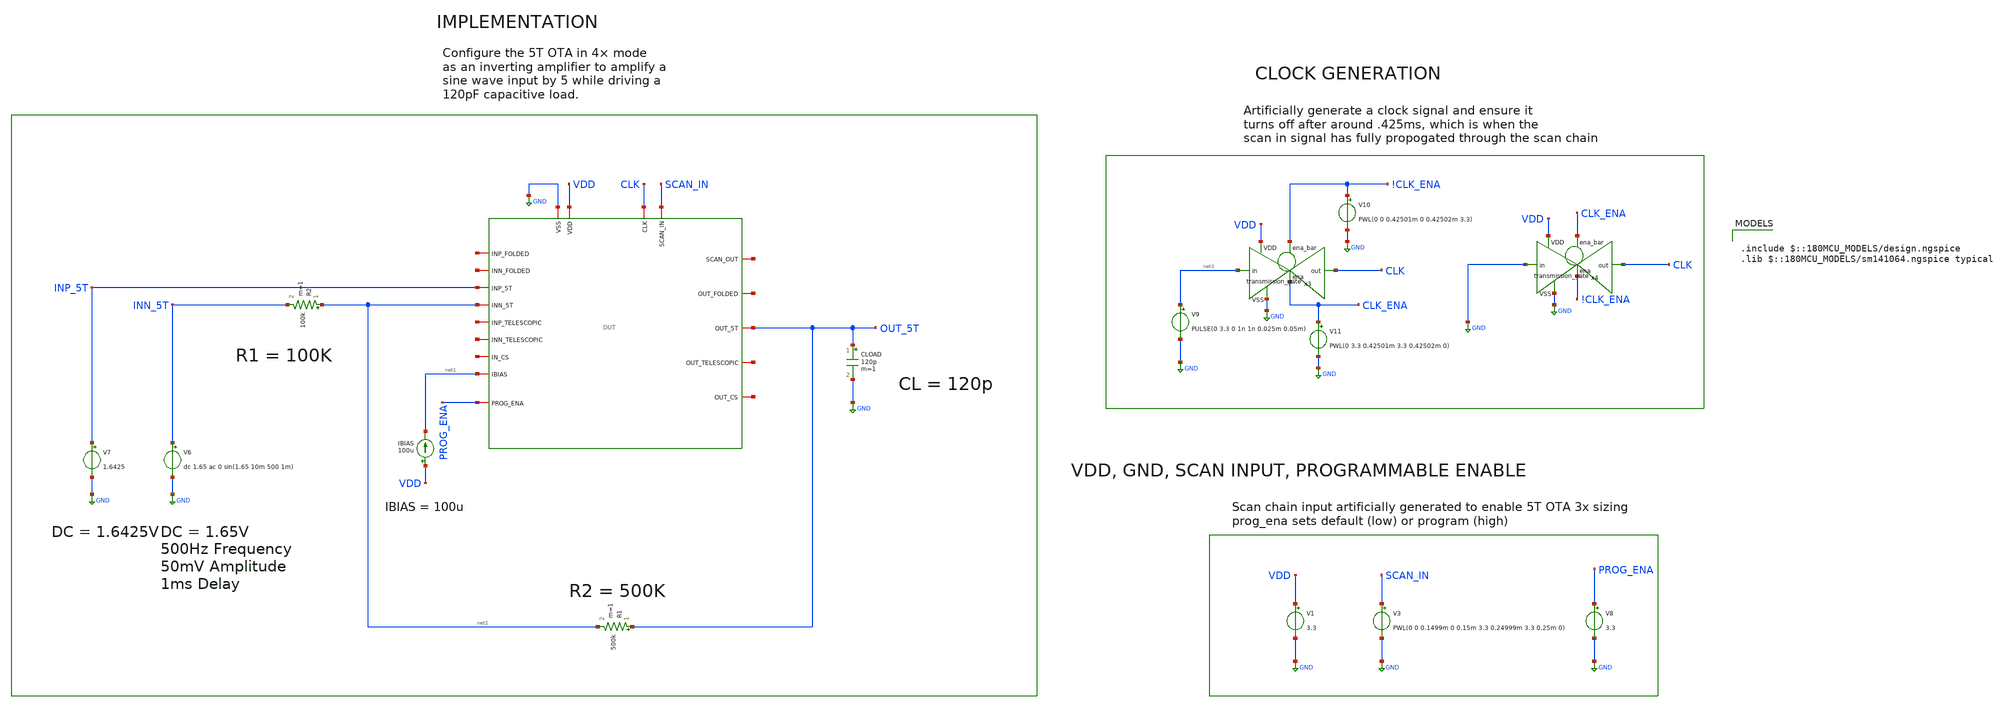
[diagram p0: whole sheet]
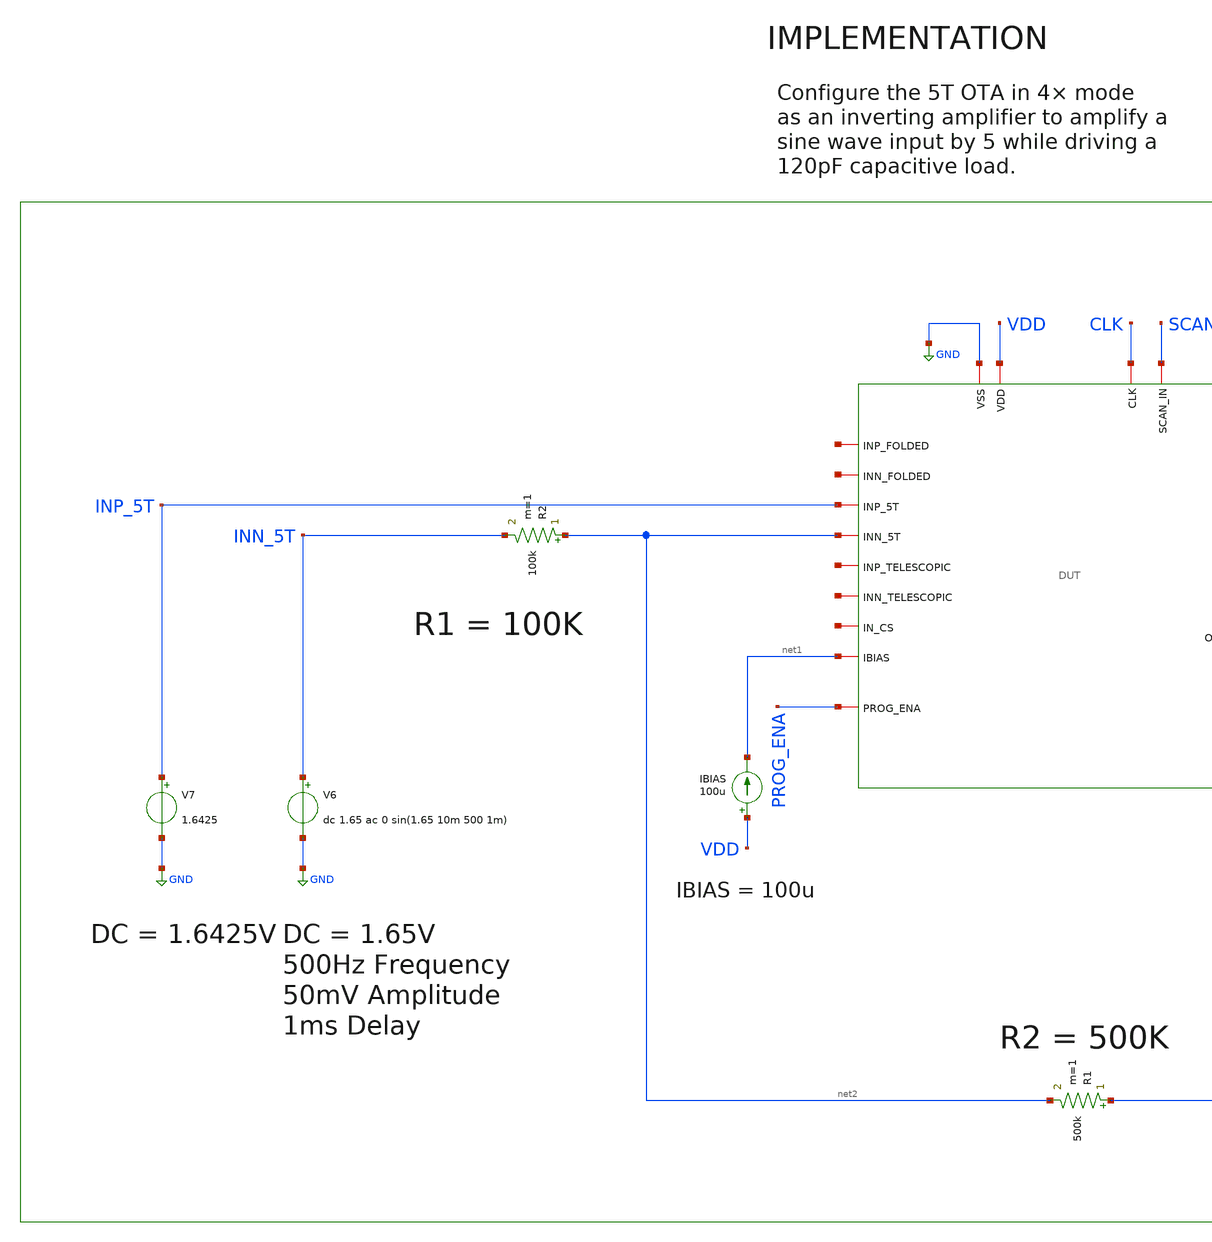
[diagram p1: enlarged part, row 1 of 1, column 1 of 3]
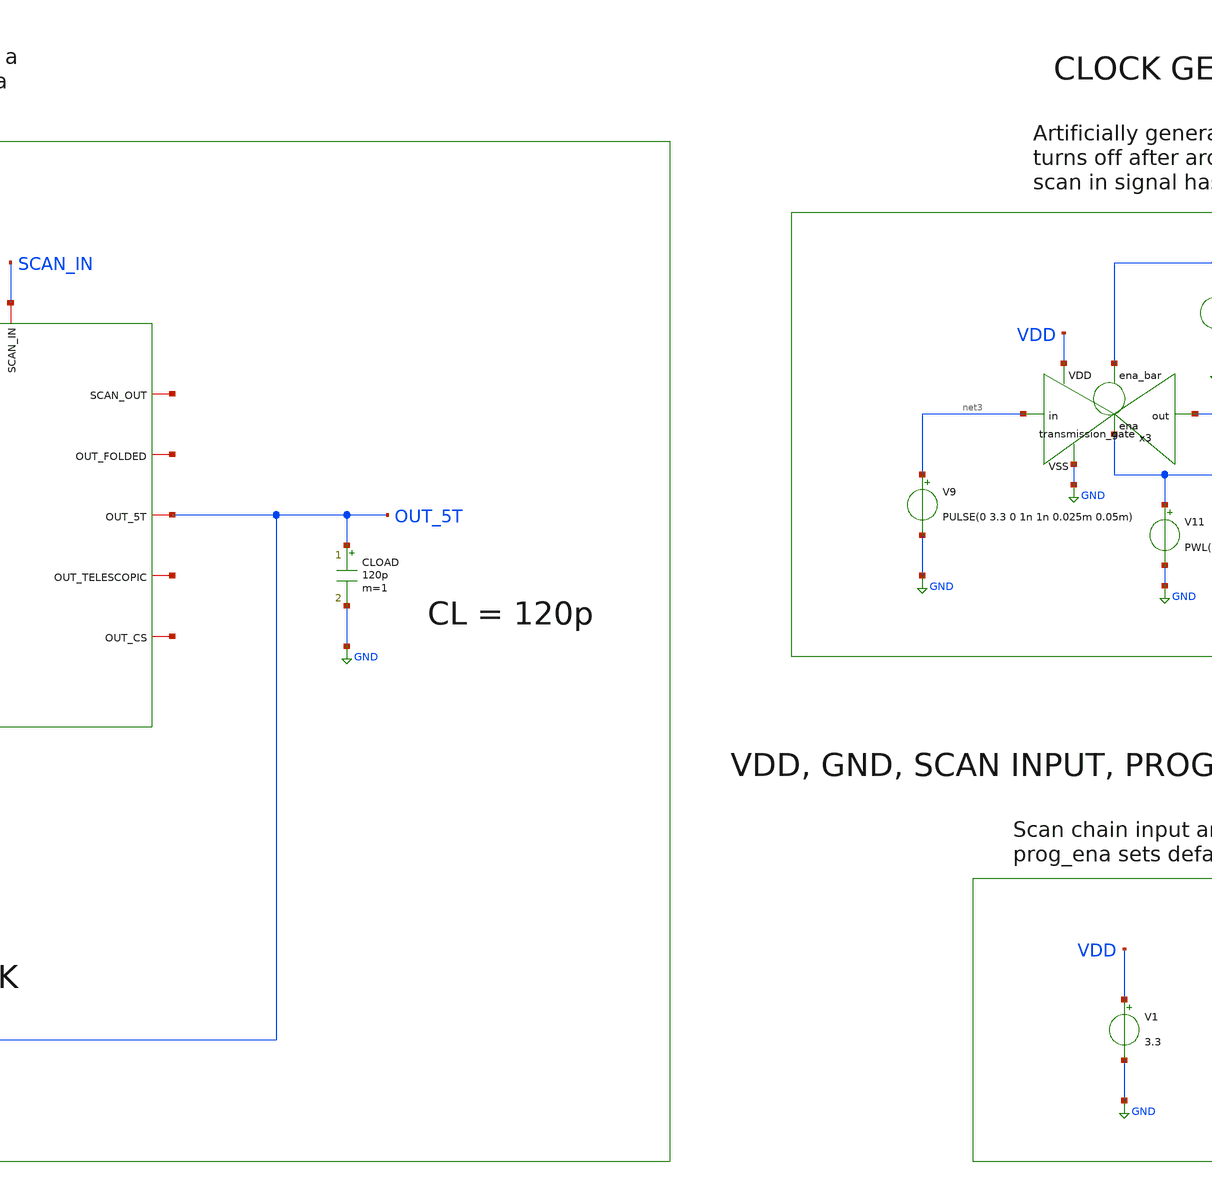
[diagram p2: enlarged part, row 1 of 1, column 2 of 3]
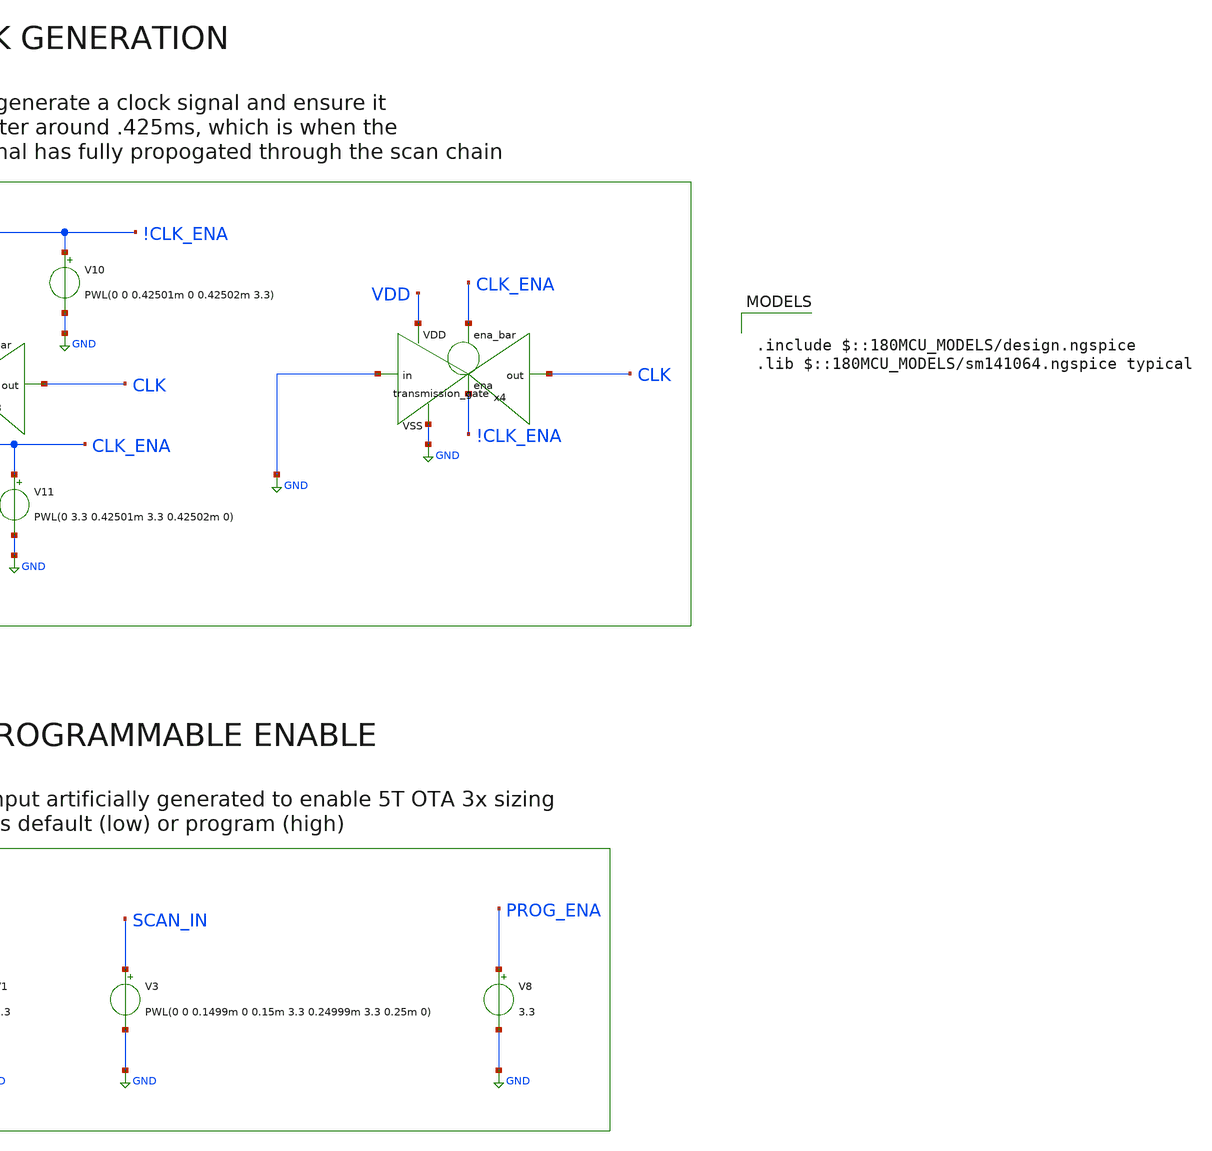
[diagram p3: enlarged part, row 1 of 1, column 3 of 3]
** sch_path: designs/libs/pex/5t/inverting_amplifier/4x.sch
**.subckt 4x
V3 SCAN_IN GND PWL(0 0 0.1499m 0 0.15m 3.3 0.24999m 3.3 0.25m 0)
V1 VDD GND 3.3
IBIAS VDD net1 100u
V7 INP_5T GND 1.6425
CLOAD OUT_5T GND 120p m=1
R2 net2 INN_5T 100k m=1
V6 INN_5T GND dc 1.65 ac 0 sin(1.65 10m 500 1m)
R1 OUT_5T net2 500k m=1
V8 PROG_ENA GND 3.3
V9 net3 GND PULSE(0 3.3 0 1n 1n 0.025m 0.05m)
x3 !CLK_ENA VDD CLK net3 GND CLK_ENA transmission_gate
V10 !CLK_ENA GND PWL(0 0 0.42501m 0 0.42502m 3.3)
V11 CLK_ENA GND PWL(0 3.3 0.42501m 3.3 0.42502m 0)
x4 CLK_ENA VDD CLK GND GND !CLK_ENA transmission_gate
x1 CLK net4 SCAN_IN GND VDD net5 net6 OUT_5T net1 net7 INP_5T net2 net8 net9 net10 net11 net12
+ PROG_ENA DUT
**** begin user architecture code

.include $::180MCU_MODELS/design.ngspice
.lib $::180MCU_MODELS/sm141064.ngspice typical



.include /foss/designs/libs/pex/DUT.spice
.control
tran 1u 5m

set color0 = white
set color1 = black

plot v(out_5T) v(inn_5T)

meas tran vout_pp pp v(out_5T) from=2m to=5m
meas tran vin_pp pp v(inn_5T) from=2m to=5m
let gain = vout_pp / vin_pp
print gain

meas tran vout_dc avg v(out_5T) from=2m to=5m
meas tran vin_dc avg v(inn_5T) from=2m to=5m
let dc_offset = vout_dc - vin_dc
let input_offset = dc_offset / 6
print vout_dc vin_dc dc_offset input_offset

let ideal_gain = 5
let gain_error_pct = (ideal_gain - gain) / ideal_gain * 100
print gain_error_pct

meas tran idd avg i(v1) from=2m to=5m
let power = abs(idd) * 3.3
print idd power
.endc


**** end user architecture code
**.ends

* expanding   symbol:  libs/core_digital/schem/transmission_gate.sym # of pins=6
** sym_path: designs/libs/core_digital/schem/transmission_gate.sym
** sch_path: designs/libs/core_digital/schem/transmission_gate.sch
.subckt transmission_gate ena_bar VDD out in VSS ena
*.ipin in
*.ipin ena_bar
*.ipin ena
*.ipin VSS
*.ipin VDD
*.opin out
XM1 in ena_bar out VDD pfet_03v3 L=0.28u W=0.22u nf=1 ad='int((nf+1)/2) * W/nf * 0.18u' as='int((nf+2)/2) * W/nf * 0.18u'
+ pd='2*int((nf+1)/2) * (W/nf + 0.18u)' ps='2*int((nf+2)/2) * (W/nf + 0.18u)' nrd='0.18u / W' nrs='0.18u / W'
+ sa=0 sb=0 sd=0 m=1
XM2 in ena out VSS nfet_03v3 L=0.28u W=0.22u nf=1 ad='int((nf+1)/2) * W/nf * 0.18u' as='int((nf+2)/2) * W/nf * 0.18u'
+ pd='2*int((nf+1)/2) * (W/nf + 0.18u)' ps='2*int((nf+2)/2) * (W/nf + 0.18u)' nrd='0.18u / W' nrs='0.18u / W'
+ sa=0 sb=0 sd=0 m=1
.ends

.GLOBAL GND
.end
